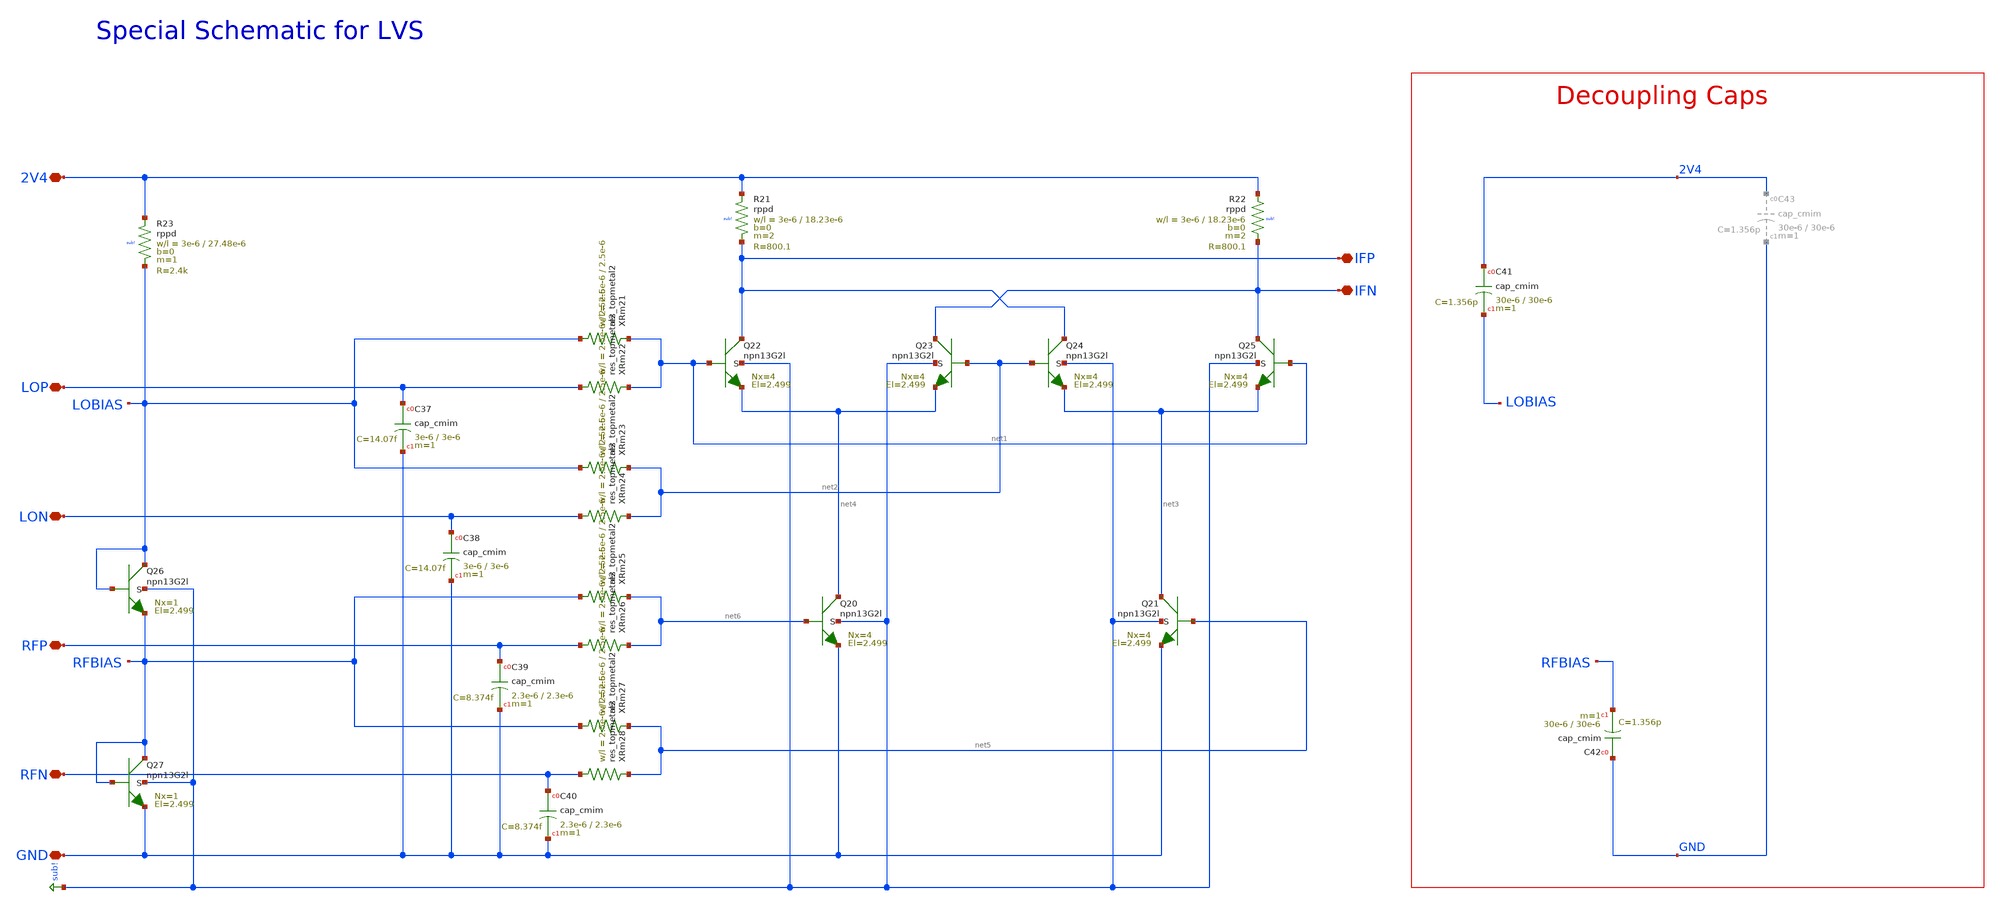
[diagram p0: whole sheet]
** sch_path: mWATTBAT/design_data/lvs/MIXER_LVS.sch
**.subckt MIXER_LVS 2V4 LOP LON RFP RFN GND IFP IFN
*.iopin 2V4
*.iopin LOP
*.iopin LON
*.iopin RFP
*.iopin RFN
*.iopin GND
*.iopin IFP
*.iopin IFN
XQ22 IFP net1 net4 sub! npn13G2l Nx=4 El=2.499 mm_ok=1
XQ23 IFN net2 net4 sub! npn13G2l Nx=4 El=2.499 mm_ok=1
XQ24 IFP net2 net3 sub! npn13G2l Nx=4 El=2.499 mm_ok=1
XQ25 IFN net1 net3 sub! npn13G2l Nx=4 El=2.499 mm_ok=1
XQ20 net4 net6 GND sub! npn13G2l Nx=4 El=2.499 mm_ok=1
XQ21 net3 net5 GND sub! npn13G2l Nx=4 El=2.499 mm_ok=1
XQ27 RFBIAS RFBIAS GND sub! npn13G2l Nx=1 El=2.499 mm_ok=1
XQ26 LOBIAS LOBIAS RFBIAS sub! npn13G2l Nx=1 El=2.499 mm_ok=1
XR21 2V4 IFP sub! rppd w=3e-6 l=18.23e-6 m=2 b=0 mm_ok=1
XR22 2V4 IFN sub! rppd w=3e-6 l=18.23e-6 m=2 b=0 mm_ok=1
XC42 GND RFBIAS cap_cmim w=30e-6 l=30e-6 m=1 mm_ok=1
XC37 LOP GND cap_cmim w=3e-6 l=3e-6 m=1 mm_ok=1
XC38 LON GND cap_cmim w=3e-6 l=3e-6 m=1 mm_ok=1
XC39 RFP GND cap_cmim w=2.3e-6 l=2.3e-6 m=1 mm_ok=1
XC40 RFN GND cap_cmim w=2.3e-6 l=2.3e-6 m=1 mm_ok=1
XR23 2V4 LOBIAS sub! rppd w=3e-6 l=27.48e-6 m=1 b=0 mm_ok=1
XC41 2V4 LOBIAS cap_cmim w=30e-6 l=30e-6 m=1 mm_ok=1
XRm21 LOBIAS net1 res_topmetal2 w=2.5e-6 l=2.5e-6
XRm22 LOP net1 res_topmetal2 w=2.5e-6 l=2.5e-6
XRm23 LOBIAS net2 res_topmetal2 w=2.5e-6 l=2.5e-6
XRm24 LON net2 res_topmetal2 w=2.5e-6 l=2.5e-6
XRm25 RFBIAS net6 res_topmetal2 w=2.5e-6 l=2.5e-6
XRm26 RFP net6 res_topmetal2 w=2.5e-6 l=2.5e-6
XRm27 RFBIAS net5 res_topmetal2 w=2.5e-6 l=2.5e-6
XRm28 RFN net5 res_topmetal2 w=2.5e-6 l=2.5e-6
**.ends
.GLOBAL sub!
.end
